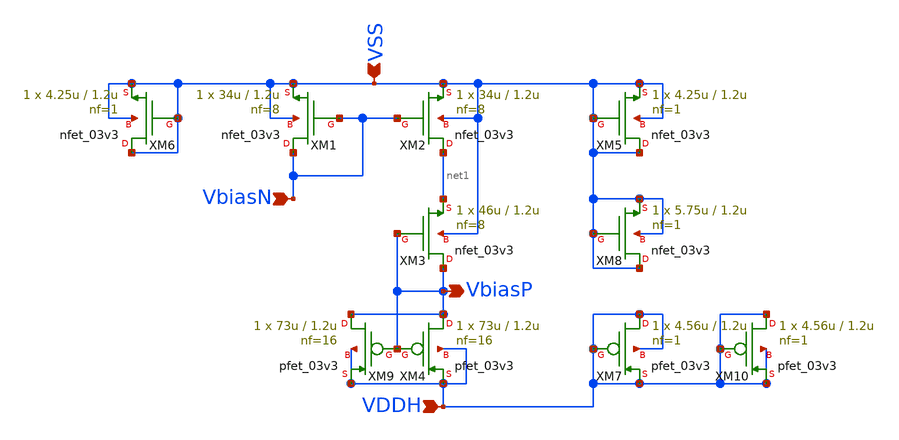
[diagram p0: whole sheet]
** sch_path: Schematics/BIAS/BIAS.sch
**.subckt BIAS VbiasN VSS VbiasP VDDH
*.ipin VbiasN
*.ipin VSS
*.opin VbiasP
*.ipin VDDH
XM1 VbiasN VbiasN VSS VSS nfet_03v3 L=1.2u W=34u nf=8 ad='int((nf+1)/2) * W/nf * 0.18u' as='int((nf+2)/2) * W/nf * 0.18u'
+ pd='2*int((nf+1)/2) * (W/nf + 0.18u)' ps='2*int((nf+2)/2) * (W/nf + 0.18u)' nrd='0.18u / W' nrs='0.18u / W'
+ sa=0 sb=0 sd=0 m=1
XM2 net1 VbiasN VSS VSS nfet_03v3 L=1.2u W=34u nf=8 ad='int((nf+1)/2) * W/nf * 0.18u' as='int((nf+2)/2) * W/nf * 0.18u'
+ pd='2*int((nf+1)/2) * (W/nf + 0.18u)' ps='2*int((nf+2)/2) * (W/nf + 0.18u)' nrd='0.18u / W' nrs='0.18u / W'
+ sa=0 sb=0 sd=0 m=1
XM3 VbiasP VbiasP net1 VSS nfet_03v3 L=1.2u W=46u nf=8 ad='int((nf+1)/2) * W/nf * 0.18u' as='int((nf+2)/2) * W/nf * 0.18u'
+ pd='2*int((nf+1)/2) * (W/nf + 0.18u)' ps='2*int((nf+2)/2) * (W/nf + 0.18u)' nrd='0.18u / W' nrs='0.18u / W'
+ sa=0 sb=0 sd=0 m=1
XM4 VbiasP VbiasP VDDH VDDH pfet_03v3 L=1.2u W=73u nf=16 ad='int((nf+1)/2) * W/nf * 0.18u' as='int((nf+2)/2) * W/nf * 0.18u'
+ pd='2*int((nf+1)/2) * (W/nf + 0.18u)' ps='2*int((nf+2)/2) * (W/nf + 0.18u)' nrd='0.18u / W' nrs='0.18u / W'
+ sa=0 sb=0 sd=0 m=1
XM5 VSS VSS VSS VSS nfet_03v3 L=1.2u W=4.25u nf=1 ad='int((nf+1)/2) * W/nf * 0.18u' as='int((nf+2)/2) * W/nf * 0.18u'
+ pd='2*int((nf+1)/2) * (W/nf + 0.18u)' ps='2*int((nf+2)/2) * (W/nf + 0.18u)' nrd='0.18u / W' nrs='0.18u / W'
+ sa=0 sb=0 sd=0 m=1
XM6 VSS VSS VSS VSS nfet_03v3 L=1.2u W=4.25u nf=1 ad='int((nf+1)/2) * W/nf * 0.18u' as='int((nf+2)/2) * W/nf * 0.18u'
+ pd='2*int((nf+1)/2) * (W/nf + 0.18u)' ps='2*int((nf+2)/2) * (W/nf + 0.18u)' nrd='0.18u / W' nrs='0.18u / W'
+ sa=0 sb=0 sd=0 m=1
XM7 VDDH VDDH VDDH VDDH pfet_03v3 L=1.2u W=4.56u nf=1 ad='int((nf+1)/2) * W/nf * 0.18u' as='int((nf+2)/2) * W/nf * 0.18u'
+ pd='2*int((nf+1)/2) * (W/nf + 0.18u)' ps='2*int((nf+2)/2) * (W/nf + 0.18u)' nrd='0.18u / W' nrs='0.18u / W'
+ sa=0 sb=0 sd=0 m=1
XM8 VSS VSS VSS VSS nfet_03v3 L=1.2u W=5.75u nf=1 ad='int((nf+1)/2) * W/nf * 0.18u' as='int((nf+2)/2) * W/nf * 0.18u'
+ pd='2*int((nf+1)/2) * (W/nf + 0.18u)' ps='2*int((nf+2)/2) * (W/nf + 0.18u)' nrd='0.18u / W' nrs='0.18u / W'
+ sa=0 sb=0 sd=0 m=1
XM9 VbiasP VbiasP VDDH VDDH pfet_03v3 L=1.2u W=73u nf=16 ad='int((nf+1)/2) * W/nf * 0.18u' as='int((nf+2)/2) * W/nf * 0.18u'
+ pd='2*int((nf+1)/2) * (W/nf + 0.18u)' ps='2*int((nf+2)/2) * (W/nf + 0.18u)' nrd='0.18u / W' nrs='0.18u / W'
+ sa=0 sb=0 sd=0 m=1
XM10 VDDH VDDH VDDH VDDH pfet_03v3 L=1.2u W=4.56u nf=1 ad='int((nf+1)/2) * W/nf * 0.18u' as='int((nf+2)/2) * W/nf * 0.18u'
+ pd='2*int((nf+1)/2) * (W/nf + 0.18u)' ps='2*int((nf+2)/2) * (W/nf + 0.18u)' nrd='0.18u / W' nrs='0.18u / W'
+ sa=0 sb=0 sd=0 m=1
**.ends
.end
